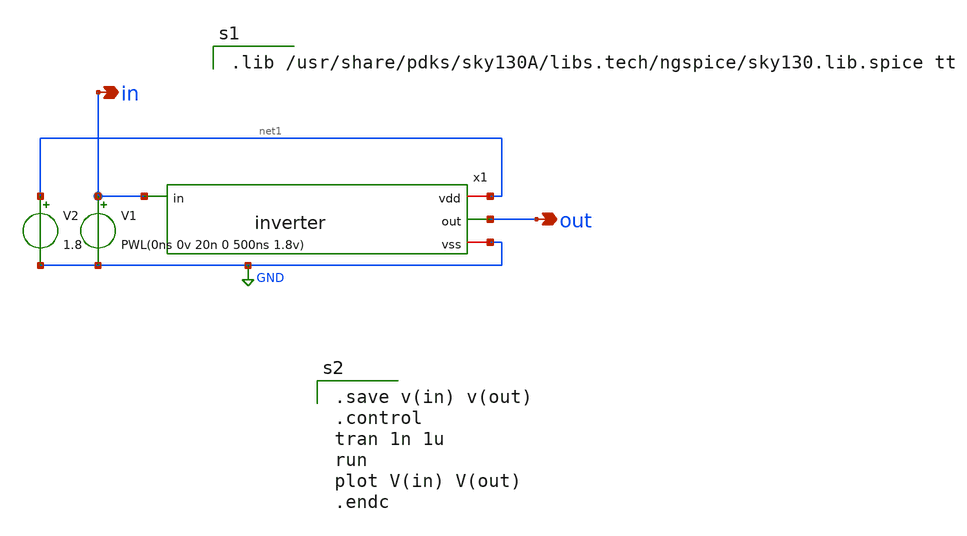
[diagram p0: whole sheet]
** sch_path: lab1/xschem/inverter_tb.sch
**.subckt inverter_tb out in
*.opin out
*.opin in
x1 net1 in out GND inverter
V1 in GND PWL(0ns 0v 20n 0 500ns 1.8v)
V2 net1 GND 1.8
**** begin user architecture code

.lib /usr/share/pdks/sky130A/libs.tech/ngspice/sky130.lib.spice tt


.save v(in) v(out)
.control
tran 1n 1u
run
plot V(in) V(out)
.endc

**** end user architecture code
**.ends

* expanding   symbol:  inverter.sym # of pins=4
** sym_path: xschem/inverter.sym
** sch_path: xschem/inverter.sch
.subckt inverter vdd in out vss
*.iopin vdd
*.iopin vss
*.ipin in
*.opin out
XM1 out in vss vss sky130_fd_pr__nfet_01v8 L=0.18 W=4.5 nf=1 ad='int((nf+1)/2) * W/nf * 0.29' as='int((nf+2)/2) * W/nf * 0.29'
+ pd='2*int((nf+1)/2) * (W/nf + 0.29)' ps='2*int((nf+2)/2) * (W/nf + 0.29)' nrd='0.29 / W' nrs='0.29 / W'
+ sa=0 sb=0 sd=0 mult=1 m=1
XM2 out in vdd vdd sky130_fd_pr__pfet_01v8 L=0.18 W=3 nf=1 ad='int((nf+1)/2) * W/nf * 0.29' as='int((nf+2)/2) * W/nf * 0.29'
+ pd='2*int((nf+1)/2) * (W/nf + 0.29)' ps='2*int((nf+2)/2) * (W/nf + 0.29)' nrd='0.29 / W' nrs='0.29 / W'
+ sa=0 sb=0 sd=0 mult=1 m=1
.ends

.GLOBAL GND
.end
